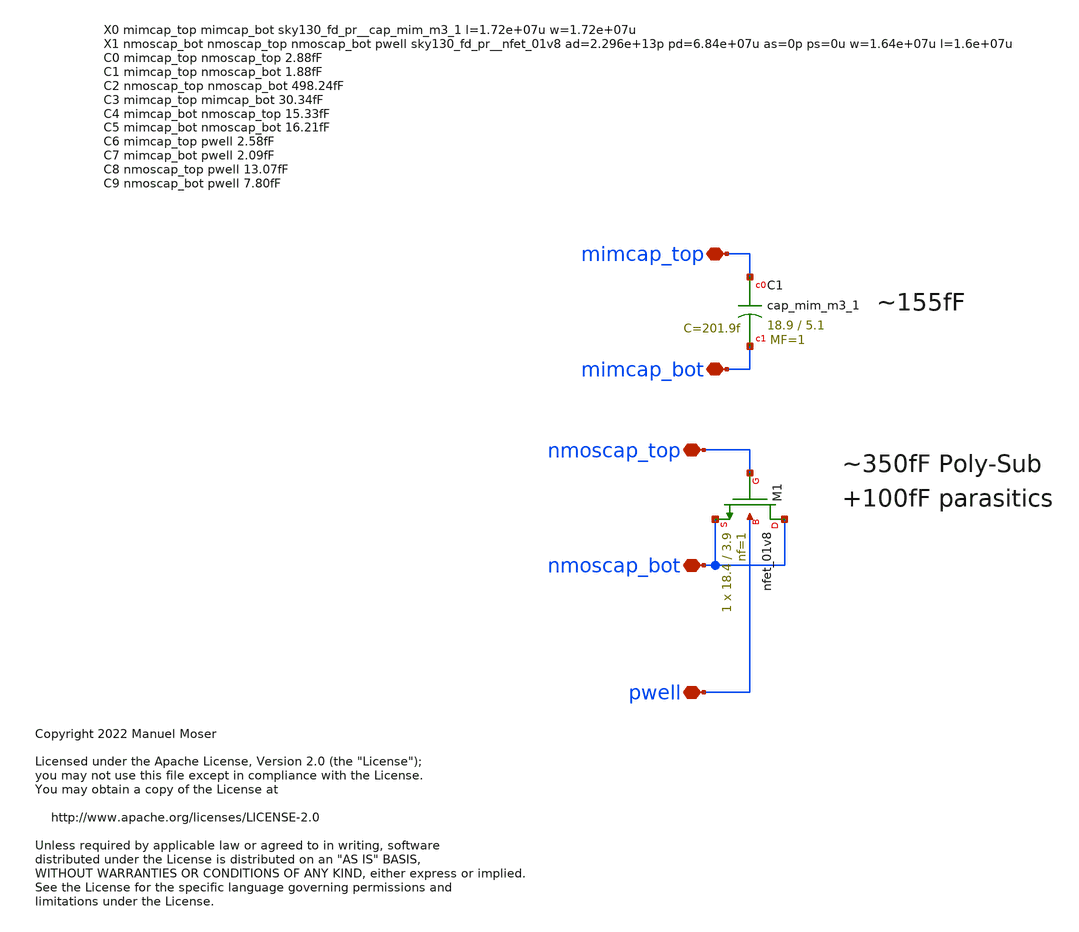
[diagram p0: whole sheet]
** sch_path: xschem/adc_noise_decoup_cell/adc_noise_decoup_cell2.sch
* Copyright 2022 Manuel Moser
* Licensed under the Apache License, Version 2.0 (the "License");
**.subckt adc_noise_decoup_cell2 nmoscap_top mimcap_top mimcap_bot nmoscap_bot pwell
*.iopin nmoscap_top
*.iopin mimcap_top
*.iopin mimcap_bot
*.iopin nmoscap_bot
*.iopin pwell
XC1 mimcap_top mimcap_bot sky130_fd_pr__cap_mim_m3_1 W=18.9 L=5.1 MF=1 m=1
XM1 nmoscap_bot nmoscap_top nmoscap_bot pwell sky130_fd_pr__nfet_01v8 L=3.9 W=18.4 nf=1 ad='int((nf+1)/2) * W/nf * 0.29'
+ as='int((nf+2)/2) * W/nf * 0.29' pd='2*int((nf+1)/2) * (W/nf + 0.29)' ps='2*int((nf+2)/2) * (W/nf + 0.29)'
+ nrd='0.29 / W' nrs='0.29 / W' sa=0 sb=0 sd=0 mult=1 m=1
**.ends
.end
